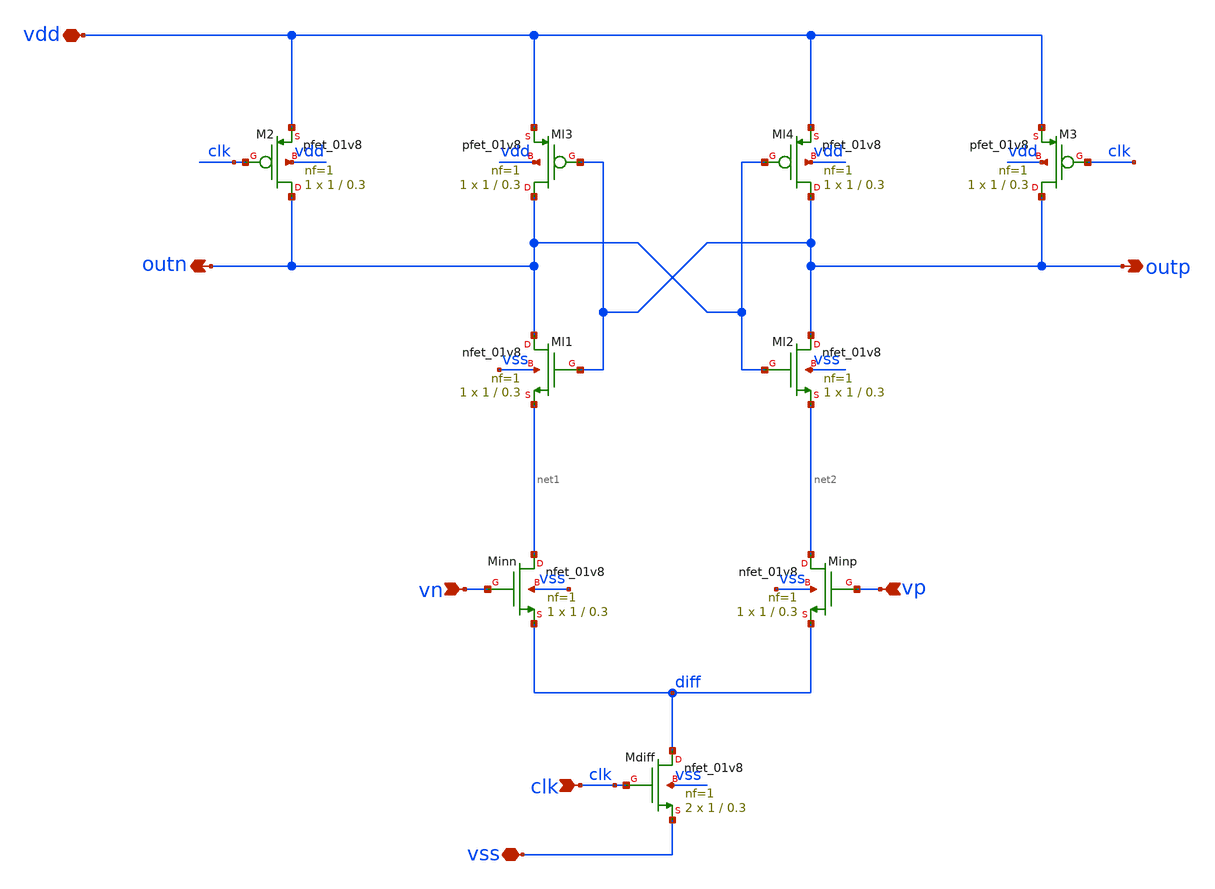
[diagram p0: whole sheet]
** sch_path: xschem/sar_10b/comparator/comparator.sch
**.subckt comparator vn vp clk vdd vss outp outn
*.ipin vn
*.ipin vp
*.ipin clk
*.iopin vdd
*.iopin vss
*.opin outp
*.opin outn
XMdiff diff clk vss vss sky130_fd_pr__nfet_01v8 L=0.3 W=1 nf=1 ad='int((nf+1)/2) * W/nf * 0.29' as='int((nf+2)/2) * W/nf * 0.29'
+ pd='2*int((nf+1)/2) * (W/nf + 0.29)' ps='2*int((nf+2)/2) * (W/nf + 0.29)' nrd='0.29 / W' nrs='0.29 / W'
+ sa=0 sb=0 sd=0 mult=2 m=2
XMinn net1 vn diff vss sky130_fd_pr__nfet_01v8 L=0.3 W=1 nf=1 ad='int((nf+1)/2) * W/nf * 0.29' as='int((nf+2)/2) * W/nf * 0.29'
+ pd='2*int((nf+1)/2) * (W/nf + 0.29)' ps='2*int((nf+2)/2) * (W/nf + 0.29)' nrd='0.29 / W' nrs='0.29 / W'
+ sa=0 sb=0 sd=0 mult=1 m=1
XMinp net2 vp diff vss sky130_fd_pr__nfet_01v8 L=0.3 W=1 nf=1 ad='int((nf+1)/2) * W/nf * 0.29' as='int((nf+2)/2) * W/nf * 0.29'
+ pd='2*int((nf+1)/2) * (W/nf + 0.29)' ps='2*int((nf+2)/2) * (W/nf + 0.29)' nrd='0.29 / W' nrs='0.29 / W'
+ sa=0 sb=0 sd=0 mult=1 m=1
XMl4 outp outn vdd vdd sky130_fd_pr__pfet_01v8 L=0.3 W=1 nf=1 ad='int((nf+1)/2) * W/nf * 0.29' as='int((nf+2)/2) * W/nf * 0.29'
+ pd='2*int((nf+1)/2) * (W/nf + 0.29)' ps='2*int((nf+2)/2) * (W/nf + 0.29)' nrd='0.29 / W' nrs='0.29 / W'
+ sa=0 sb=0 sd=0 mult=1 m=1
XMl3 outn outp vdd vdd sky130_fd_pr__pfet_01v8 L=0.3 W=1 nf=1 ad='int((nf+1)/2) * W/nf * 0.29' as='int((nf+2)/2) * W/nf * 0.29'
+ pd='2*int((nf+1)/2) * (W/nf + 0.29)' ps='2*int((nf+2)/2) * (W/nf + 0.29)' nrd='0.29 / W' nrs='0.29 / W'
+ sa=0 sb=0 sd=0 mult=1 m=1
XM3 outp clk vdd vdd sky130_fd_pr__pfet_01v8 L=0.3 W=1 nf=1 ad='int((nf+1)/2) * W/nf * 0.29' as='int((nf+2)/2) * W/nf * 0.29'
+ pd='2*int((nf+1)/2) * (W/nf + 0.29)' ps='2*int((nf+2)/2) * (W/nf + 0.29)' nrd='0.29 / W' nrs='0.29 / W'
+ sa=0 sb=0 sd=0 mult=1 m=1
XM2 outn clk vdd vdd sky130_fd_pr__pfet_01v8 L=0.3 W=1 nf=1 ad='int((nf+1)/2) * W/nf * 0.29' as='int((nf+2)/2) * W/nf * 0.29'
+ pd='2*int((nf+1)/2) * (W/nf + 0.29)' ps='2*int((nf+2)/2) * (W/nf + 0.29)' nrd='0.29 / W' nrs='0.29 / W'
+ sa=0 sb=0 sd=0 mult=1 m=1
XMl1 outn outp net1 vss sky130_fd_pr__nfet_01v8 L=0.3 W=1 nf=1 ad='int((nf+1)/2) * W/nf * 0.29' as='int((nf+2)/2) * W/nf * 0.29'
+ pd='2*int((nf+1)/2) * (W/nf + 0.29)' ps='2*int((nf+2)/2) * (W/nf + 0.29)' nrd='0.29 / W' nrs='0.29 / W'
+ sa=0 sb=0 sd=0 mult=1 m=1
XMl2 outp outn net2 vss sky130_fd_pr__nfet_01v8 L=0.3 W=1 nf=1 ad='int((nf+1)/2) * W/nf * 0.29' as='int((nf+2)/2) * W/nf * 0.29'
+ pd='2*int((nf+1)/2) * (W/nf + 0.29)' ps='2*int((nf+2)/2) * (W/nf + 0.29)' nrd='0.29 / W' nrs='0.29 / W'
+ sa=0 sb=0 sd=0 mult=1 m=1
**.ends
.end
